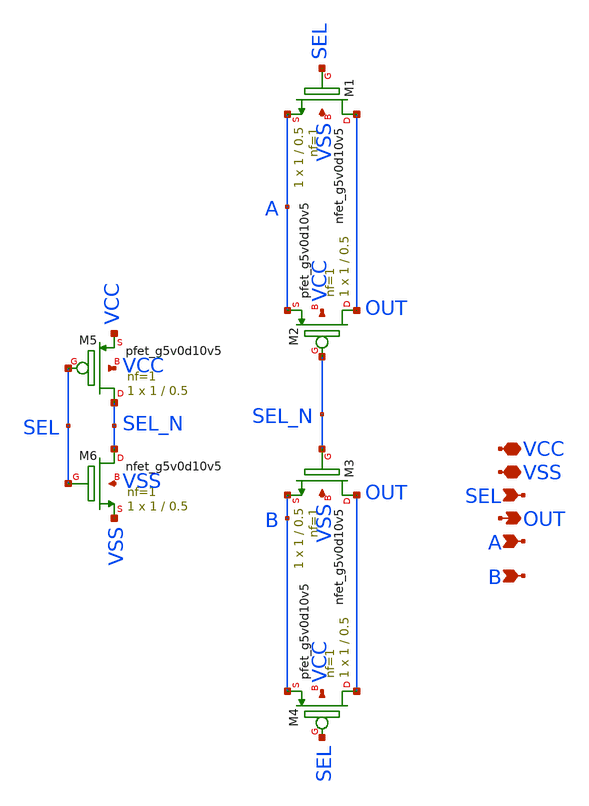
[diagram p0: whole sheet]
** sch_path: Comparator/schematic/self_calibrating/Mux.sch
**.subckt Mux VCC SEL OUT VSS A B
*.iopin VCC
*.ipin SEL
*.opin OUT
*.iopin VSS
*.ipin A
*.ipin B
XM1 OUT SEL A VSS sky130_fd_pr__nfet_g5v0d10v5 L=0.5 W=1 nf=1 ad='int((nf+1)/2) * W/nf * 0.29' as='int((nf+2)/2) * W/nf * 0.29'
+ pd='2*int((nf+1)/2) * (W/nf + 0.29)' ps='2*int((nf+2)/2) * (W/nf + 0.29)' nrd='0.29 / W' nrs='0.29 / W'
+ sa=0 sb=0 sd=0 mult=1 m=1
XM2 OUT SEL_N A VCC sky130_fd_pr__pfet_g5v0d10v5 L=0.5 W=1 nf=1 ad='int((nf+1)/2) * W/nf * 0.29' as='int((nf+2)/2) * W/nf * 0.29'
+ pd='2*int((nf+1)/2) * (W/nf + 0.29)' ps='2*int((nf+2)/2) * (W/nf + 0.29)' nrd='0.29 / W' nrs='0.29 / W'
+ sa=0 sb=0 sd=0 mult=1 m=1
XM3 OUT SEL_N B VSS sky130_fd_pr__nfet_g5v0d10v5 L=0.5 W=1 nf=1 ad='int((nf+1)/2) * W/nf * 0.29' as='int((nf+2)/2) * W/nf * 0.29'
+ pd='2*int((nf+1)/2) * (W/nf + 0.29)' ps='2*int((nf+2)/2) * (W/nf + 0.29)' nrd='0.29 / W' nrs='0.29 / W'
+ sa=0 sb=0 sd=0 mult=1 m=1
XM4 OUT SEL B VCC sky130_fd_pr__pfet_g5v0d10v5 L=0.5 W=1 nf=1 ad='int((nf+1)/2) * W/nf * 0.29' as='int((nf+2)/2) * W/nf * 0.29'
+ pd='2*int((nf+1)/2) * (W/nf + 0.29)' ps='2*int((nf+2)/2) * (W/nf + 0.29)' nrd='0.29 / W' nrs='0.29 / W'
+ sa=0 sb=0 sd=0 mult=1 m=1
XM5 SEL_N SEL VCC VCC sky130_fd_pr__pfet_g5v0d10v5 L=0.5 W=1 nf=1 ad='int((nf+1)/2) * W/nf * 0.29' as='int((nf+2)/2) * W/nf * 0.29'
+ pd='2*int((nf+1)/2) * (W/nf + 0.29)' ps='2*int((nf+2)/2) * (W/nf + 0.29)' nrd='0.29 / W' nrs='0.29 / W'
+ sa=0 sb=0 sd=0 mult=1 m=1
XM6 SEL_N SEL VSS VSS sky130_fd_pr__nfet_g5v0d10v5 L=0.5 W=1 nf=1 ad='int((nf+1)/2) * W/nf * 0.29' as='int((nf+2)/2) * W/nf * 0.29'
+ pd='2*int((nf+1)/2) * (W/nf + 0.29)' ps='2*int((nf+2)/2) * (W/nf + 0.29)' nrd='0.29 / W' nrs='0.29 / W'
+ sa=0 sb=0 sd=0 mult=1 m=1
**.ends
.end
